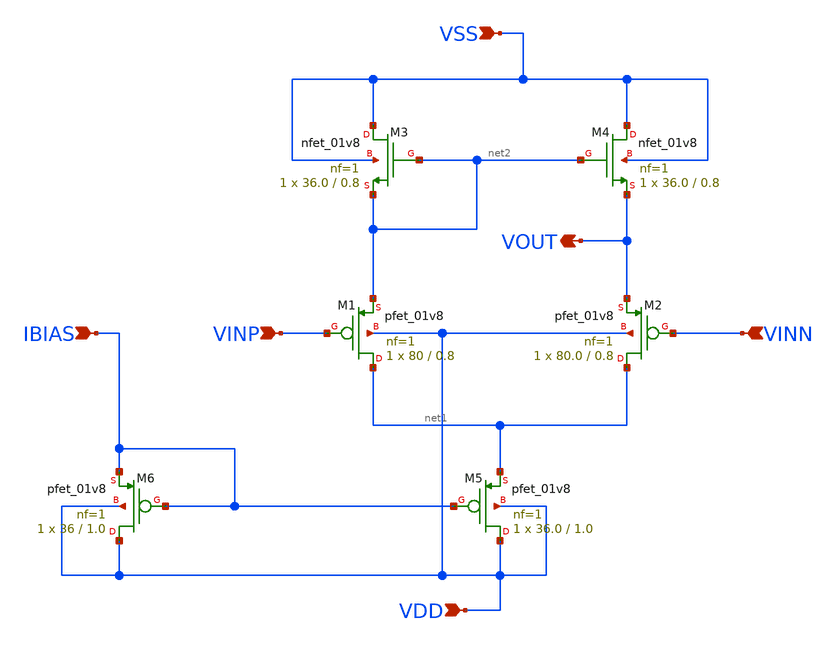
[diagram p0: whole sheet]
** sch_path: lelo_5tota_pmos_sky130a/design/LELO_5TOTA_PMOS_SKY130A/LELO_5TOTA_PMOS.sch
**.subckt LELO_5TOTA_PMOS VSS VDD VOUT IBIAS VINP VINN
*.ipin VSS
*.ipin VDD
*.opin VOUT
*.ipin IBIAS
*.ipin VINP
*.ipin VINN
XM2 net1 VINN VOUT VDD sky130_fd_pr__pfet_01v8 L=0.8 W=80.0 nf=1 ad='int((1 + 1)/2) * 80.0 / 1 * 0.29'
+ as='int((1 + 2)/2) * 80.0 / 1 * 0.29' pd='2*int((1 + 1)/2) * (80.0 / 1 + 0.29)' ps='2*int((1 + 2)/2) * (80.0 / 1 + 0.29)'
+ nrd='0.29 / 80.0 ' nrs='0.29 / 80.0 ' sa=0 sb=0 sd=0 mult=1 m=1
XM4 VSS net2 VOUT VSS sky130_fd_pr__nfet_01v8 L=0.8 W=36.0 nf=1 ad='int((1 + 1)/2) * 36.0 / 1 * 0.29'
+ as='int((1 + 2)/2) * 36.0 / 1 * 0.29' pd='2*int((1 + 1)/2) * (36.0 / 1 + 0.29)' ps='2*int((1 + 2)/2) * (36.0 / 1 + 0.29)'
+ nrd='0.29 / 36.0 ' nrs='0.29 / 36.0 ' sa=0 sb=0 sd=0 mult=1 m=1
XM3 VSS net2 net2 VSS sky130_fd_pr__nfet_01v8 L=0.8 W=36.0 nf=1 ad='int((1 + 1)/2) * 36.0 / 1 * 0.29'
+ as='int((1 + 2)/2) * 36.0 / 1 * 0.29' pd='2*int((1 + 1)/2) * (36.0 / 1 + 0.29)' ps='2*int((1 + 2)/2) * (36.0 / 1 + 0.29)'
+ nrd='0.29 / 36.0 ' nrs='0.29 / 36.0 ' sa=0 sb=0 sd=0 mult=1 m=1
XM6 VDD IBIAS IBIAS VDD sky130_fd_pr__pfet_01v8 L=1.0 W=36 nf=1 ad='int((1 + 1)/2) * 36 / 1 * 0.29' as='int((1 + 2)/2) * 36 / 1 * 0.29'
+ pd='2*int((1 + 1)/2) * (36 / 1 + 0.29)' ps='2*int((1 + 2)/2) * (36 / 1 + 0.29)' nrd='0.29 / 36 ' nrs='0.29 / 36 '
+ sa=0 sb=0 sd=0 mult=1 m=1
XM1 net1 VINP net2 VDD sky130_fd_pr__pfet_01v8 L=0.8 W=80 nf=1 ad='int((1 + 1)/2) * 80 / 1 * 0.29' as='int((1 + 2)/2) * 80 / 1 * 0.29'
+ pd='2*int((1 + 1)/2) * (80 / 1 + 0.29)' ps='2*int((1 + 2)/2) * (80 / 1 + 0.29)' nrd='0.29 / 80 ' nrs='0.29 / 80 '
+ sa=0 sb=0 sd=0 mult=1 m=1
XM5 VDD IBIAS net1 VDD sky130_fd_pr__pfet_01v8 L=1.0 W=36.0 nf=1 ad='int((1 + 1)/2) * 36.0 / 1 * 0.29'
+ as='int((1 + 2)/2) * 36.0 / 1 * 0.29' pd='2*int((1 + 1)/2) * (36.0 / 1 + 0.29)' ps='2*int((1 + 2)/2) * (36.0 / 1 + 0.29)'
+ nrd='0.29 / 36.0 ' nrs='0.29 / 36.0 ' sa=0 sb=0 sd=0 mult=1 m=1
**.ends
.end
